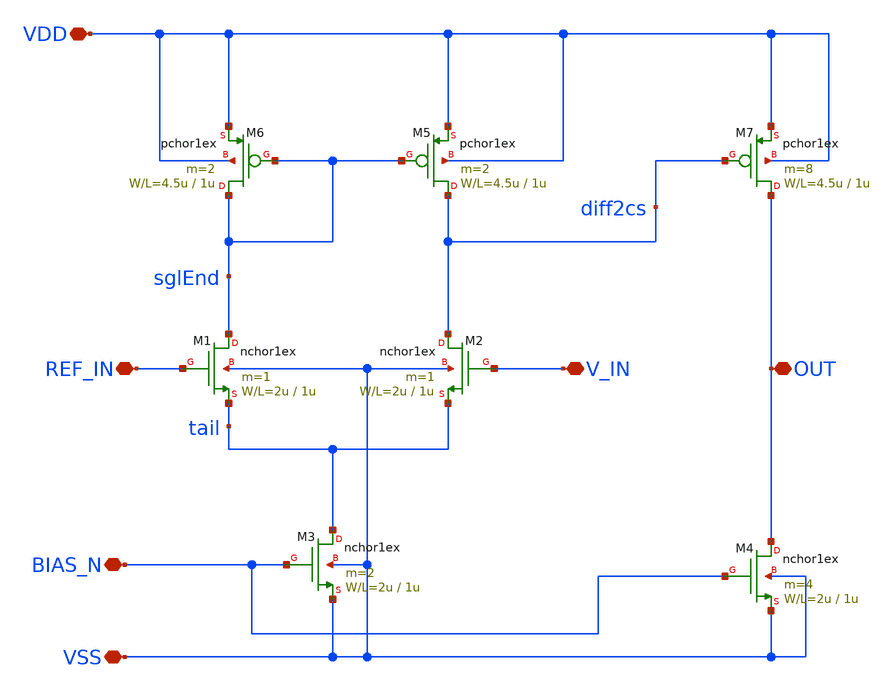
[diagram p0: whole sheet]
** sch_path: design/.design_bk/xschem/VCO/SA_DIV_CompNch.sch
**.subckt SA_DIV_CompNch VDD VSS BIAS_N REF_IN V_IN OUT
*.iopin VDD
*.iopin VSS
*.iopin BIAS_N
*.iopin REF_IN
*.iopin V_IN
*.iopin OUT
M1 sglEnd REF_IN tail VSS nchor1ex L=1u W=2u m=1
M2 diff2cs V_IN tail VSS nchor1ex L=1u W=2u m=1
M3 tail BIAS_N VSS VSS nchor1ex L=1u W=2u m=2
M4 OUT BIAS_N VSS VSS nchor1ex L=1u W=2u m=4
M5 diff2cs sglEnd VDD VDD pchor1ex L=1u W=4.5u m=2
M6 sglEnd sglEnd VDD VDD pchor1ex L=1u W=4.5u m=2
M7 OUT diff2cs VDD VDD pchor1ex L=1u W=4.5u m=8
**.ends
.end
